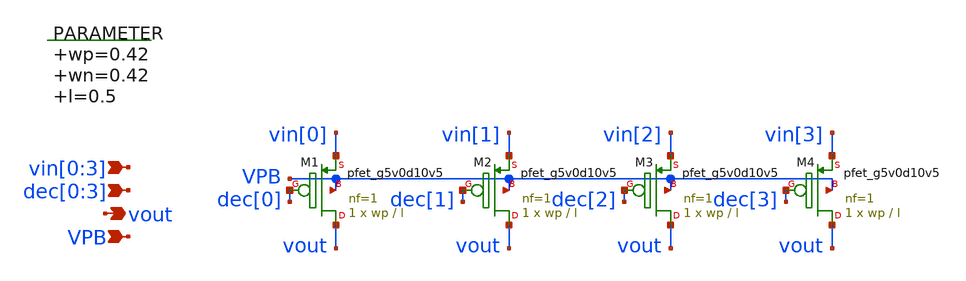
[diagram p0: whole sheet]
** sch_path: xschem/vselector_6b_1v_stage_3_pmos.sch
**.subckt vselector_6b_1v_stage_3_pmos vin[0],vin[1],vin[2],vin[3] vout VPB
*+ dec[0],dec[1],dec[2],dec[3]
*.ipin vin[0],vin[1],vin[2],vin[3]
*.opin vout
*.ipin VPB
*.ipin dec[0],dec[1],dec[2],dec[3]
.param wp=0.42 wn=0.42 l=0.5

XM1 vout dec[0] vin[0] VPB sky130_fd_pr__pfet_g5v0d10v5 L=l W=wp nf=1 ad='int((nf+1)/2) * W/nf * 0.29'
+ as='int((nf+2)/2) * W/nf * 0.29' pd='2*int((nf+1)/2) * (W/nf + 0.29)' ps='2*int((nf+2)/2) * (W/nf + 0.29)'
+ nrd='0.29 / W' nrs='0.29 / W' sa=0 sb=0 sd=0 mult=1 m=1
XM2 vout dec[1] vin[1] VPB sky130_fd_pr__pfet_g5v0d10v5 L=l W=wp nf=1 ad='int((nf+1)/2) * W/nf * 0.29'
+ as='int((nf+2)/2) * W/nf * 0.29' pd='2*int((nf+1)/2) * (W/nf + 0.29)' ps='2*int((nf+2)/2) * (W/nf + 0.29)'
+ nrd='0.29 / W' nrs='0.29 / W' sa=0 sb=0 sd=0 mult=1 m=1
XM3 vout dec[2] vin[2] VPB sky130_fd_pr__pfet_g5v0d10v5 L=l W=wp nf=1 ad='int((nf+1)/2) * W/nf * 0.29'
+ as='int((nf+2)/2) * W/nf * 0.29' pd='2*int((nf+1)/2) * (W/nf + 0.29)' ps='2*int((nf+2)/2) * (W/nf + 0.29)'
+ nrd='0.29 / W' nrs='0.29 / W' sa=0 sb=0 sd=0 mult=1 m=1
XM4 vout dec[3] vin[3] VPB sky130_fd_pr__pfet_g5v0d10v5 L=l W=wp nf=1 ad='int((nf+1)/2) * W/nf * 0.29'
+ as='int((nf+2)/2) * W/nf * 0.29' pd='2*int((nf+1)/2) * (W/nf + 0.29)' ps='2*int((nf+2)/2) * (W/nf + 0.29)'
+ nrd='0.29 / W' nrs='0.29 / W' sa=0 sb=0 sd=0 mult=1 m=1
**.ends
.end
